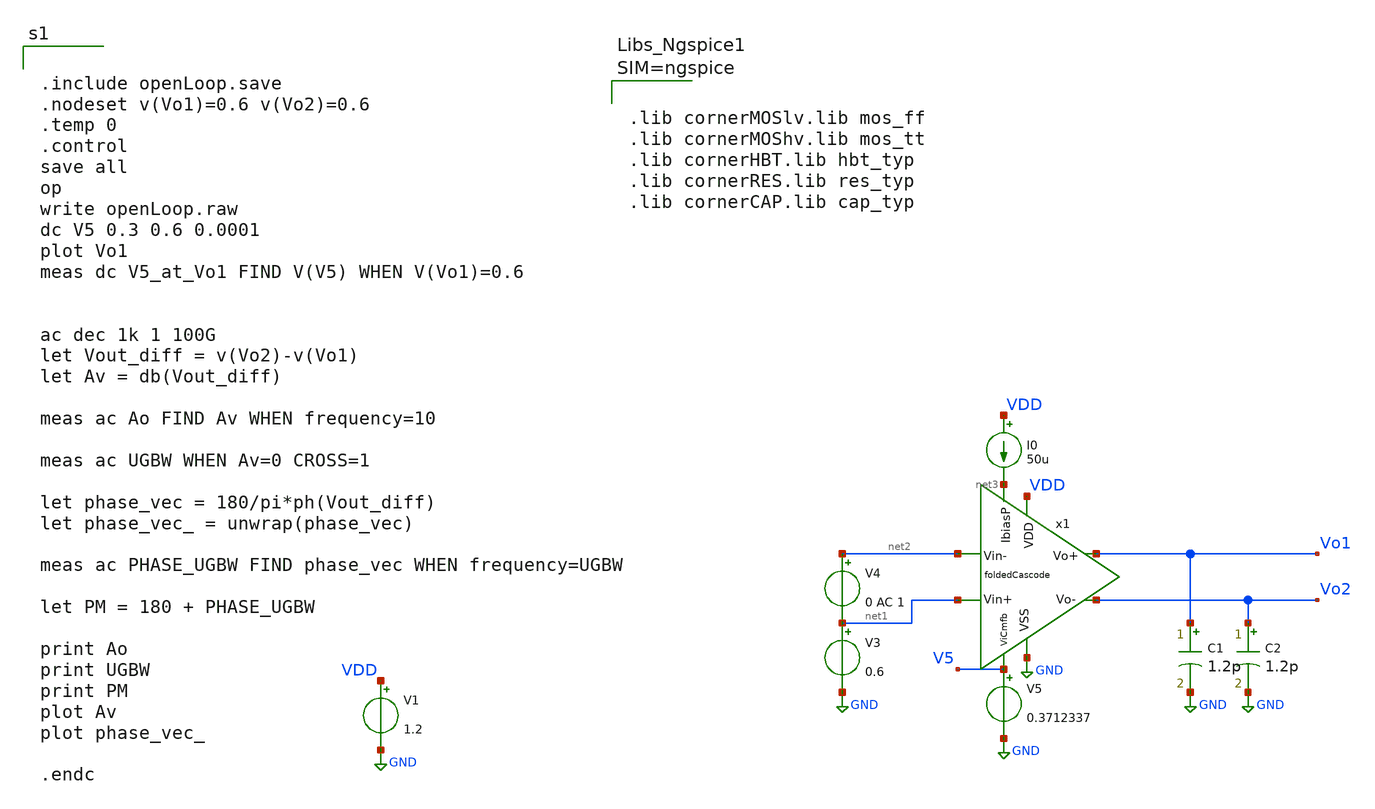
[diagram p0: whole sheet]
** sch_path: sch/tb/openLoop.sch
**.subckt openLoop
x1 VDD GND V5 net3 Vo1 Vo2 net2 net1 foldedCascode
V1 VDD GND 1.2
V3 net1 GND 0.6
V4 net2 net1 0 AC 1
C1 Vo1 GND 1.2p m=1
C2 Vo2 GND 1.2p m=1
V5 V5 GND 0.3712337
I0 VDD net3 50u
**** begin user architecture code


.include openLoop.save
.nodeset v(Vo1)=0.6 v(Vo2)=0.6
.temp 0
.control
save all
op
write openLoop.raw
dc V5 0.3 0.6 0.0001
plot Vo1
meas dc V5_at_Vo1 FIND V(V5) WHEN V(Vo1)=0.6


ac dec 1k 1 100G
let Vout_diff = v(Vo2)-v(Vo1)
let Av = db(Vout_diff)

meas ac Ao FIND Av WHEN frequency=10

meas ac UGBW WHEN Av=0 CROSS=1

let phase_vec = 180/pi*ph(Vout_diff)
let phase_vec_ = unwrap(phase_vec)

meas ac PHASE_UGBW FIND phase_vec WHEN frequency=UGBW

let PM = 180 + PHASE_UGBW

print Ao
print UGBW
print PM
plot Av
plot phase_vec_

.endc





.lib cornerMOSlv.lib mos_ff
.lib cornerMOShv.lib mos_tt
.lib cornerHBT.lib hbt_typ
.lib cornerRES.lib res_typ
.lib cornerCAP.lib cap_typ



**** end user architecture code
**.ends

* expanding   symbol:  foldedCascode.sym # of pins=8
** sym_path: sch/blocks/foldedCascode.sym
** sch_path: sch/blocks/foldedCascode.sch
.subckt foldedCascode VDD VSS ViCmfb IbiasP Vo+ Vo- Vin- Vin+
*.iopin VSS
*.iopin VDD
*.ipin ViCmfb
*.iopin IbiasP
*.ipin Vin+
*.ipin Vin-
*.iopin Vo+
*.iopin Vo-
x1 VDD Vb1_1 Vb1_2 Vx Vy VSS gmBoosting
XM0 net3 Vb0 VDD VDD sg13_lv_pmos w=70u l=0.3u ng=120 m=8 mm_ok=1
XM1 Vy Vin+ net3 net3 sg13_lv_pmos w=70u l=0.13u ng=100 m=2 mm_ok=1
XM2 Vx Vin- net3 net3 sg13_lv_pmos w=70u l=0.13u ng=100 m=2 mm_ok=1
XM7 Vo+ Vb2 net1 VDD sg13_lv_pmos w=47u l=0.4u ng=94 m=4 mm_ok=1
XM3 Vo+ Vb1_1 Vx VSS sg13_lv_nmos w=44u l=0.3u ng=22 m=6 mm_ok=1
XM8 Vo- Vb2 net2 VDD sg13_lv_pmos w=47u l=0.4u ng=94 m=4 mm_ok=1
XM12 Vx ViCmfb VSS VSS sg13_lv_nmos w=24.2u l=0.8u ng=62 m=6 mm_ok=1
XM4 Vo- Vb1_2 Vy VSS sg13_lv_nmos w=44u l=0.3u ng=22 m=6 mm_ok=1
XM5 Vy ViCmfb VSS VSS sg13_lv_nmos w=24.2u l=0.8u ng=62 m=6 mm_ok=1
I0 Vb0 VSS 10u
XM6 Vb0 Vb0 net4 VDD sg13_lv_pmos w=60u l=0.13u ng=10 m=1 mm_ok=1
XM13 net4 Vb0 VDD VDD sg13_lv_pmos w=11.5u l=0.3u ng=5 m=1 mm_ok=1
I1 Vb2 VSS 25u
XM18 Vb2 Vb2 net5 VDD sg13_lv_pmos w=18.5u l=0.7u ng=9 m=1 mm_ok=1
XM19 net5 Vb2 VDD VDD sg13_lv_pmos w=4u l=0.7u ng=1 m=1 mm_ok=1
XM20 Vb3 Vb2 net6 VDD sg13_lv_pmos w=5.5u l=0.4u ng=1 m=1 mm_ok=1
XM21 net6 Vb3 VDD VDD sg13_lv_pmos w=8.1u l=0.8u ng=1 m=1 mm_ok=1
I2 Vb3 VSS 10u
XM11 IbiasP IbiasP VSS VSS sg13_lv_nmos w=44u l=0.3u ng=22 m=6 mm_ok=1
XM9 net1 Vb3 VDD VDD sg13_lv_pmos w=62.2u l=0.8u ng=118 m=4 mm_ok=1
XM10 net2 Vb3 VDD VDD sg13_lv_pmos w=62.2u l=0.8u ng=118 m=4 mm_ok=1
.ends


* expanding   symbol:  gmBoosting.sym # of pins=6
** sym_path: sch/blocks/gmBoosting.sym
** sch_path: sch/blocks/gmBoosting.sch
.subckt gmBoosting VDD Vo2 Vo1 Vi+ Vi- VSS
*.iopin VSS
*.opin Vo1
*.opin Vo2
*.ipin Vi+
*.ipin Vi-
*.iopin VDD
XM7 net2 Vb4 VDD VDD sg13_lv_pmos w=19.8u l=0.7u ng=20 m=2 mm_ok=1
XM1 net8 Vi+ net1 net1 sg13_lv_pmos w=35u l=0.15u ng=70 m=4 mm_ok=1
XM2 net4 Vi- net1 net1 sg13_lv_pmos w=35u l=0.15u ng=70 m=4 mm_ok=1
XM0 net1 Vb0 net5 VDD sg13_lv_pmos w=12u l=0.3u ng=12 m=1 mm_ok=1
XM6 net8 Vb3 VSS VSS sg13_lv_nmos w=20.2u l=0.7u ng=5 m=2 mm_ok=1
XM9 Vo1 Vb2 net2 VDD sg13_lv_pmos w=23.2u l=0.3u ng=10 m=1 mm_ok=1
XM10 Vo2 Vb2 net3 VDD sg13_lv_pmos w=23.2u l=0.3u ng=10 m=1 mm_ok=1
XM3 net5 Vo2 VDD VDD sg13_lv_pmos w=20u l=0.13u ng=5 m=1 mm_ok=1
XM4 net5 Vo1 VDD VDD sg13_lv_pmos w=20u l=0.13u ng=5 m=1 mm_ok=1
XM5 net6 Va VDD VDD sg13_lv_pmos w=20u l=0.13u ng=5 m=2 mm_ok=1
XM28 Vb0 net7 VSS VSS sg13_lv_nmos w=10u l=0.2u ng=2 m=1 mm_ok=1
XM29 Vb3 Vb3 VSS VSS sg13_lv_nmos w=32u l=0.7u ng=4 m=1 mm_ok=1
XR16 net7 Vb0 sub! rppd w=0.8e-6 l=2.5e-6 m=1 b=0 mm_ok=1
XM30 Vb3 Vb0 net6 VDD sg13_lv_pmos w=12u l=0.3u ng=12 m=1 mm_ok=1
XM31 net4 Vb3 VSS VSS sg13_lv_nmos w=20.2u l=0.7u ng=5 m=2 mm_ok=1
XM32 Vo1 Vb1 net4 VSS sg13_lv_nmos w=38.7u l=0.6u ng=5 m=1 mm_ok=1
XM23 net7 VbbP VDD VDD sg13_lv_pmos w=18u l=1u ng=18 m=1 mm_ok=1
I3 VbbP VSS 50u
XM21 VbbP VbbP VDD VDD sg13_lv_pmos w=18u l=1u ng=18 m=1 mm_ok=1
XM24 VbbN VbbP VDD VDD sg13_lv_pmos w=18u l=1u ng=18 m=1 mm_ok=1
XM25 VbbN VbbN VSS VSS sg13_lv_nmos w=15u l=1u ng=2 m=1 mm_ok=1
XM17 Va VbbN VSS VSS sg13_lv_nmos w=15u l=1u ng=2 m=1 mm_ok=1
XM18 Va Va VDD VDD sg13_lv_pmos w=13u l=1u ng=13 m=1 mm_ok=1
XM19 Vb1 Vb1 net10 VSS sg13_lv_nmos w=13u l=0.7u ng=2 m=1 mm_ok=1
XM20 net10 Vb1 VSS VSS sg13_lv_nmos w=2.4u l=0.7u ng=1 m=1 mm_ok=1
XM22 Vb1 VbbP VDD VDD sg13_lv_pmos w=18u l=1u ng=18 m=1 mm_ok=1
XM26 Vb4 Vb2 net9 VDD sg13_lv_pmos w=9u l=0.3u ng=9 m=1 mm_ok=1
XM38 net9 Vb4 VDD VDD sg13_lv_pmos w=15.5u l=0.7u ng=15 m=1 mm_ok=1
XM39 Vb4 VbbN VSS VSS sg13_lv_nmos w=15u l=1u ng=2 m=1 mm_ok=1
XM40 net11 Vb2 VDD VDD sg13_lv_pmos w=4.5u l=0.7u ng=1 m=1 mm_ok=1
XM41 Vb2 Vb2 net11 VDD sg13_lv_pmos w=15u l=0.7u ng=15 m=1 mm_ok=1
XM42 Vb2 VbbN VSS VSS sg13_lv_nmos w=15u l=1u ng=2 m=1 mm_ok=1
XM8 net3 Vb4 VDD VDD sg13_lv_pmos w=19.8u l=0.7u ng=20 m=2 mm_ok=1
XM11 Vo2 Vb1 net8 VSS sg13_lv_nmos w=38.7u l=0.6u ng=5 m=1 mm_ok=1
.ends

.GLOBAL GND
.end
